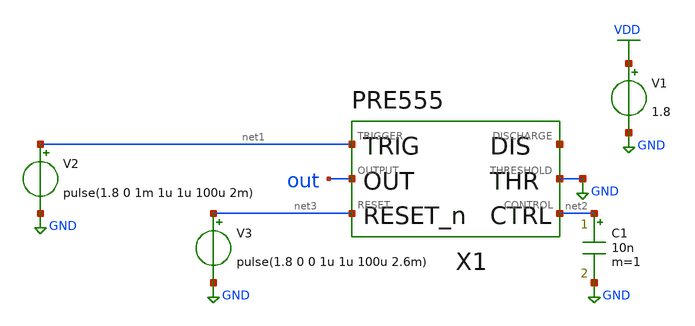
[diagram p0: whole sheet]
** sch_path: xschem/bistable_tb.sch
**.subckt bistable_tb
X1 net1 out net3 GND net4 net2 pre555
V1 VDD GND 1.8
C1 net2 GND 10n m=1
V2 net1 GND pulse(1.8 0 1m 1u 1u 100u 2m)
V3 net3 GND pulse(1.8 0 0 1u 1u 100u 2.6m)
**** begin user architecture code


.option wnflag=1
.lib /usr/local/share/pdk/sky130A/libs.tech/ngspice/sky130.lib.spice tt
.param MC_MM_SWITCH=1.0
.tran 1u 5m


**** end user architecture code
**.ends

* expanding   symbol:  pre555.sym # of pins=6
** sym_path: xschem/pre555.sym
** sch_path: xschem/pre555.sch
.subckt pre555 TRIGGER OUTPUT RESET THRESHOLD DISCHARGE CONTROL
*.opin OUTPUT
*.iopin DISCHARGE
*.ipin TRIGGER
*.ipin THRESHOLD
*.ipin CONTROL
*.ipin RESET
X1 net1 CONTROL vdiv
X2 THRESHOLD CONTROL net3 comp
X3 net1 TRIGGER net2 comp
X4 net2 net3 OUTPUT net4 net5 sr_latch
XM1 DISCHARGE net4 GND GND sky130_fd_pr__nfet_01v8 L=0.15 W=5 nf=1 ad='int((1 + 1)/2) * 5 / 1 * 0.29'
+ as='int((1 + 2)/2) * 5 / 1 * 0.29' pd='2*int((1 + 1)/2) * (5 / 1 + 0.29)' ps='2*int((1 + 2)/2) * (5 / 1 + 0.29)'
+ nrd='0.29 / 5 ' nrs='0.29 / 5 ' sa=0 sb=0 sd=0 mult=1 m=1
X5 RESET net5 inverter
.ends


* expanding   symbol:  vdiv.sym # of pins=2
** sym_path: xschem/vdiv.sym
** sch_path: xschem/vdiv.sch
.subckt vdiv v1t v2t
*.iopin v2t
*.iopin v1t
XR1 v2t VDD res100k
XR2 v1t v2t res100k
XR3 GND v1t res100k
.ends


* expanding   symbol:  comp.sym # of pins=3
** sym_path: xschem/comp.sym
** sch_path: xschem/comp.sch
.subckt comp inp inn out
*.ipin inp
*.ipin inn
*.opin out
XM1 net1 inn net3 GND sky130_fd_pr__nfet_01v8 L=1 W=1 nf=1 ad='int((1 + 1)/2) * 1 / 1 * 0.29' as='int((1 + 2)/2) * 1 / 1 * 0.29'
+ pd='2*int((1 + 1)/2) * (1 / 1 + 0.29)' ps='2*int((1 + 2)/2) * (1 / 1 + 0.29)' nrd='0.29 / 1 ' nrs='0.29 / 1 '
+ sa=0 sb=0 sd=0 mult=1 m=1
XM2 net1 net1 VDD VDD sky130_fd_pr__pfet_01v8 L=1 W=1 nf=1 ad='int((1 + 1)/2) * 1 / 1 * 0.29' as='int((1 + 2)/2) * 1 / 1 * 0.29'
+ pd='2*int((1 + 1)/2) * (1 / 1 + 0.29)' ps='2*int((1 + 2)/2) * (1 / 1 + 0.29)' nrd='0.29 / 1 ' nrs='0.29 / 1 '
+ sa=0 sb=0 sd=0 mult=1 m=1
XM3 net2 net1 VDD VDD sky130_fd_pr__pfet_01v8 L=1 W=1 nf=1 ad='int((1 + 1)/2) * 1 / 1 * 0.29' as='int((1 + 2)/2) * 1 / 1 * 0.29'
+ pd='2*int((1 + 1)/2) * (1 / 1 + 0.29)' ps='2*int((1 + 2)/2) * (1 / 1 + 0.29)' nrd='0.29 / 1 ' nrs='0.29 / 1 '
+ sa=0 sb=0 sd=0 mult=1 m=1
XM4 net2 inp net3 GND sky130_fd_pr__nfet_01v8 L=1 W=1 nf=1 ad='int((1 + 1)/2) * 1 / 1 * 0.29' as='int((1 + 2)/2) * 1 / 1 * 0.29'
+ pd='2*int((1 + 1)/2) * (1 / 1 + 0.29)' ps='2*int((1 + 2)/2) * (1 / 1 + 0.29)' nrd='0.29 / 1 ' nrs='0.29 / 1 '
+ sa=0 sb=0 sd=0 mult=1 m=1
XM5 net3 net4 GND GND sky130_fd_pr__nfet_01v8 L=1 W=3.5 nf=1 ad='int((1 + 1)/2) * 3.5 / 1 * 0.29' as='int((1 + 2)/2) * 3.5 / 1 * 0.29'
+ pd='2*int((1 + 1)/2) * (3.5 / 1 + 0.29)' ps='2*int((1 + 2)/2) * (3.5 / 1 + 0.29)' nrd='0.29 / 3.5 ' nrs='0.29 / 3.5 '
+ sa=0 sb=0 sd=0 mult=1 m=1
XM6 net4 net4 GND GND sky130_fd_pr__nfet_01v8 L=1 W=3.5 nf=1 ad='int((1 + 1)/2) * 3.5 / 1 * 0.29' as='int((1 + 2)/2) * 3.5 / 1 * 0.29'
+ pd='2*int((1 + 1)/2) * (3.5 / 1 + 0.29)' ps='2*int((1 + 2)/2) * (3.5 / 1 + 0.29)' nrd='0.29 / 3.5 ' nrs='0.29 / 3.5 '
+ sa=0 sb=0 sd=0 mult=1 m=1
XR1 net4 VDD res100k
X1 net2 out inverter
.ends


* expanding   symbol:  sr_latch.sym # of pins=5
** sym_path: xschem/sr_latch.sym
** sch_path: xschem/sr_latch.sch
.subckt sr_latch s r0 q qn r1
*.ipin s
*.ipin r0
*.opin qn
*.opin q
*.ipin r1
XM1 qn q net1 VDD sky130_fd_pr__pfet_01v8 L=0.15 W=1 nf=1 ad='int((1 + 1)/2) * 1 / 1 * 0.29' as='int((1 + 2)/2) * 1 / 1 * 0.29'
+ pd='2*int((1 + 1)/2) * (1 / 1 + 0.29)' ps='2*int((1 + 2)/2) * (1 / 1 + 0.29)' nrd='0.29 / 1 ' nrs='0.29 / 1 '
+ sa=0 sb=0 sd=0 mult=1 m=1
XM2 net1 s VDD VDD sky130_fd_pr__pfet_01v8 L=0.15 W=1 nf=1 ad='int((1 + 1)/2) * 1 / 1 * 0.29' as='int((1 + 2)/2) * 1 / 1 * 0.29'
+ pd='2*int((1 + 1)/2) * (1 / 1 + 0.29)' ps='2*int((1 + 2)/2) * (1 / 1 + 0.29)' nrd='0.29 / 1 ' nrs='0.29 / 1 '
+ sa=0 sb=0 sd=0 mult=1 m=1
XM3 qn s GND GND sky130_fd_pr__nfet_01v8 L=0.15 W=1 nf=1 ad='int((1 + 1)/2) * 1 / 1 * 0.29' as='int((1 + 2)/2) * 1 / 1 * 0.29'
+ pd='2*int((1 + 1)/2) * (1 / 1 + 0.29)' ps='2*int((1 + 2)/2) * (1 / 1 + 0.29)' nrd='0.29 / 1 ' nrs='0.29 / 1 '
+ sa=0 sb=0 sd=0 mult=1 m=1
XM4 qn q GND GND sky130_fd_pr__nfet_01v8 L=0.15 W=1 nf=1 ad='int((1 + 1)/2) * 1 / 1 * 0.29' as='int((1 + 2)/2) * 1 / 1 * 0.29'
+ pd='2*int((1 + 1)/2) * (1 / 1 + 0.29)' ps='2*int((1 + 2)/2) * (1 / 1 + 0.29)' nrd='0.29 / 1 ' nrs='0.29 / 1 '
+ sa=0 sb=0 sd=0 mult=1 m=1
XM5 q qn net2 VDD sky130_fd_pr__pfet_01v8 L=0.15 W=1 nf=1 ad='int((1 + 1)/2) * 1 / 1 * 0.29' as='int((1 + 2)/2) * 1 / 1 * 0.29'
+ pd='2*int((1 + 1)/2) * (1 / 1 + 0.29)' ps='2*int((1 + 2)/2) * (1 / 1 + 0.29)' nrd='0.29 / 1 ' nrs='0.29 / 1 '
+ sa=0 sb=0 sd=0 mult=1 m=1
XM6 net2 r0 net3 VDD sky130_fd_pr__pfet_01v8 L=0.15 W=1 nf=1 ad='int((1 + 1)/2) * 1 / 1 * 0.29' as='int((1 + 2)/2) * 1 / 1 * 0.29'
+ pd='2*int((1 + 1)/2) * (1 / 1 + 0.29)' ps='2*int((1 + 2)/2) * (1 / 1 + 0.29)' nrd='0.29 / 1 ' nrs='0.29 / 1 '
+ sa=0 sb=0 sd=0 mult=1 m=1
XM7 q r0 GND GND sky130_fd_pr__nfet_01v8 L=0.15 W=1 nf=1 ad='int((1 + 1)/2) * 1 / 1 * 0.29' as='int((1 + 2)/2) * 1 / 1 * 0.29'
+ pd='2*int((1 + 1)/2) * (1 / 1 + 0.29)' ps='2*int((1 + 2)/2) * (1 / 1 + 0.29)' nrd='0.29 / 1 ' nrs='0.29 / 1 '
+ sa=0 sb=0 sd=0 mult=1 m=1
XM8 q qn GND GND sky130_fd_pr__nfet_01v8 L=0.15 W=1 nf=1 ad='int((1 + 1)/2) * 1 / 1 * 0.29' as='int((1 + 2)/2) * 1 / 1 * 0.29'
+ pd='2*int((1 + 1)/2) * (1 / 1 + 0.29)' ps='2*int((1 + 2)/2) * (1 / 1 + 0.29)' nrd='0.29 / 1 ' nrs='0.29 / 1 '
+ sa=0 sb=0 sd=0 mult=1 m=1
XM9 net3 r1 VDD VDD sky130_fd_pr__pfet_01v8 L=0.15 W=1 nf=1 ad='int((1 + 1)/2) * 1 / 1 * 0.29' as='int((1 + 2)/2) * 1 / 1 * 0.29'
+ pd='2*int((1 + 1)/2) * (1 / 1 + 0.29)' ps='2*int((1 + 2)/2) * (1 / 1 + 0.29)' nrd='0.29 / 1 ' nrs='0.29 / 1 '
+ sa=0 sb=0 sd=0 mult=1 m=1
XM10 q r1 GND GND sky130_fd_pr__nfet_01v8 L=0.15 W=1 nf=1 ad='int((1 + 1)/2) * 1 / 1 * 0.29' as='int((1 + 2)/2) * 1 / 1 * 0.29'
+ pd='2*int((1 + 1)/2) * (1 / 1 + 0.29)' ps='2*int((1 + 2)/2) * (1 / 1 + 0.29)' nrd='0.29 / 1 ' nrs='0.29 / 1 '
+ sa=0 sb=0 sd=0 mult=1 m=1
.ends


* expanding   symbol:  inverter.sym # of pins=2
** sym_path: xschem/inverter.sym
** sch_path: xschem/inverter.sch
.subckt inverter a y
*.ipin a
*.opin y
XM1 y a GND GND sky130_fd_pr__nfet_01v8 L=0.15 W=1 nf=1 ad='int((1 + 1)/2) * 1 / 1 * 0.29' as='int((1 + 2)/2) * 1 / 1 * 0.29'
+ pd='2*int((1 + 1)/2) * (1 / 1 + 0.29)' ps='2*int((1 + 2)/2) * (1 / 1 + 0.29)' nrd='0.29 / 1 ' nrs='0.29 / 1 '
+ sa=0 sb=0 sd=0 mult=1 m=1
XM2 y a VDD VDD sky130_fd_pr__pfet_01v8 L=0.15 W=1 nf=1 ad='int((1 + 1)/2) * 1 / 1 * 0.29' as='int((1 + 2)/2) * 1 / 1 * 0.29'
+ pd='2*int((1 + 1)/2) * (1 / 1 + 0.29)' ps='2*int((1 + 2)/2) * (1 / 1 + 0.29)' nrd='0.29 / 1 ' nrs='0.29 / 1 '
+ sa=0 sb=0 sd=0 mult=1 m=1
.ends


* expanding   symbol:  res100k.sym # of pins=2
** sym_path: xschem/res100k.sym
** sch_path: xschem/res100k.sch
.subckt res100k bot top
*.iopin top
*.iopin bot
XR1 net1 top GND sky130_fd_pr__res_xhigh_po_0p35 L=3.5 mult=1 m=1
XR2 net2 net1 GND sky130_fd_pr__res_xhigh_po_0p35 L=3.5 mult=1 m=1
XR3 net3 net2 GND sky130_fd_pr__res_xhigh_po_0p35 L=3.5 mult=1 m=1
XR4 net4 net3 GND sky130_fd_pr__res_xhigh_po_0p35 L=3.5 mult=1 m=1
XR5 bot net4 GND sky130_fd_pr__res_xhigh_po_0p35 L=3.5 mult=1 m=1
.ends

.GLOBAL GND
.GLOBAL VDD
.end
